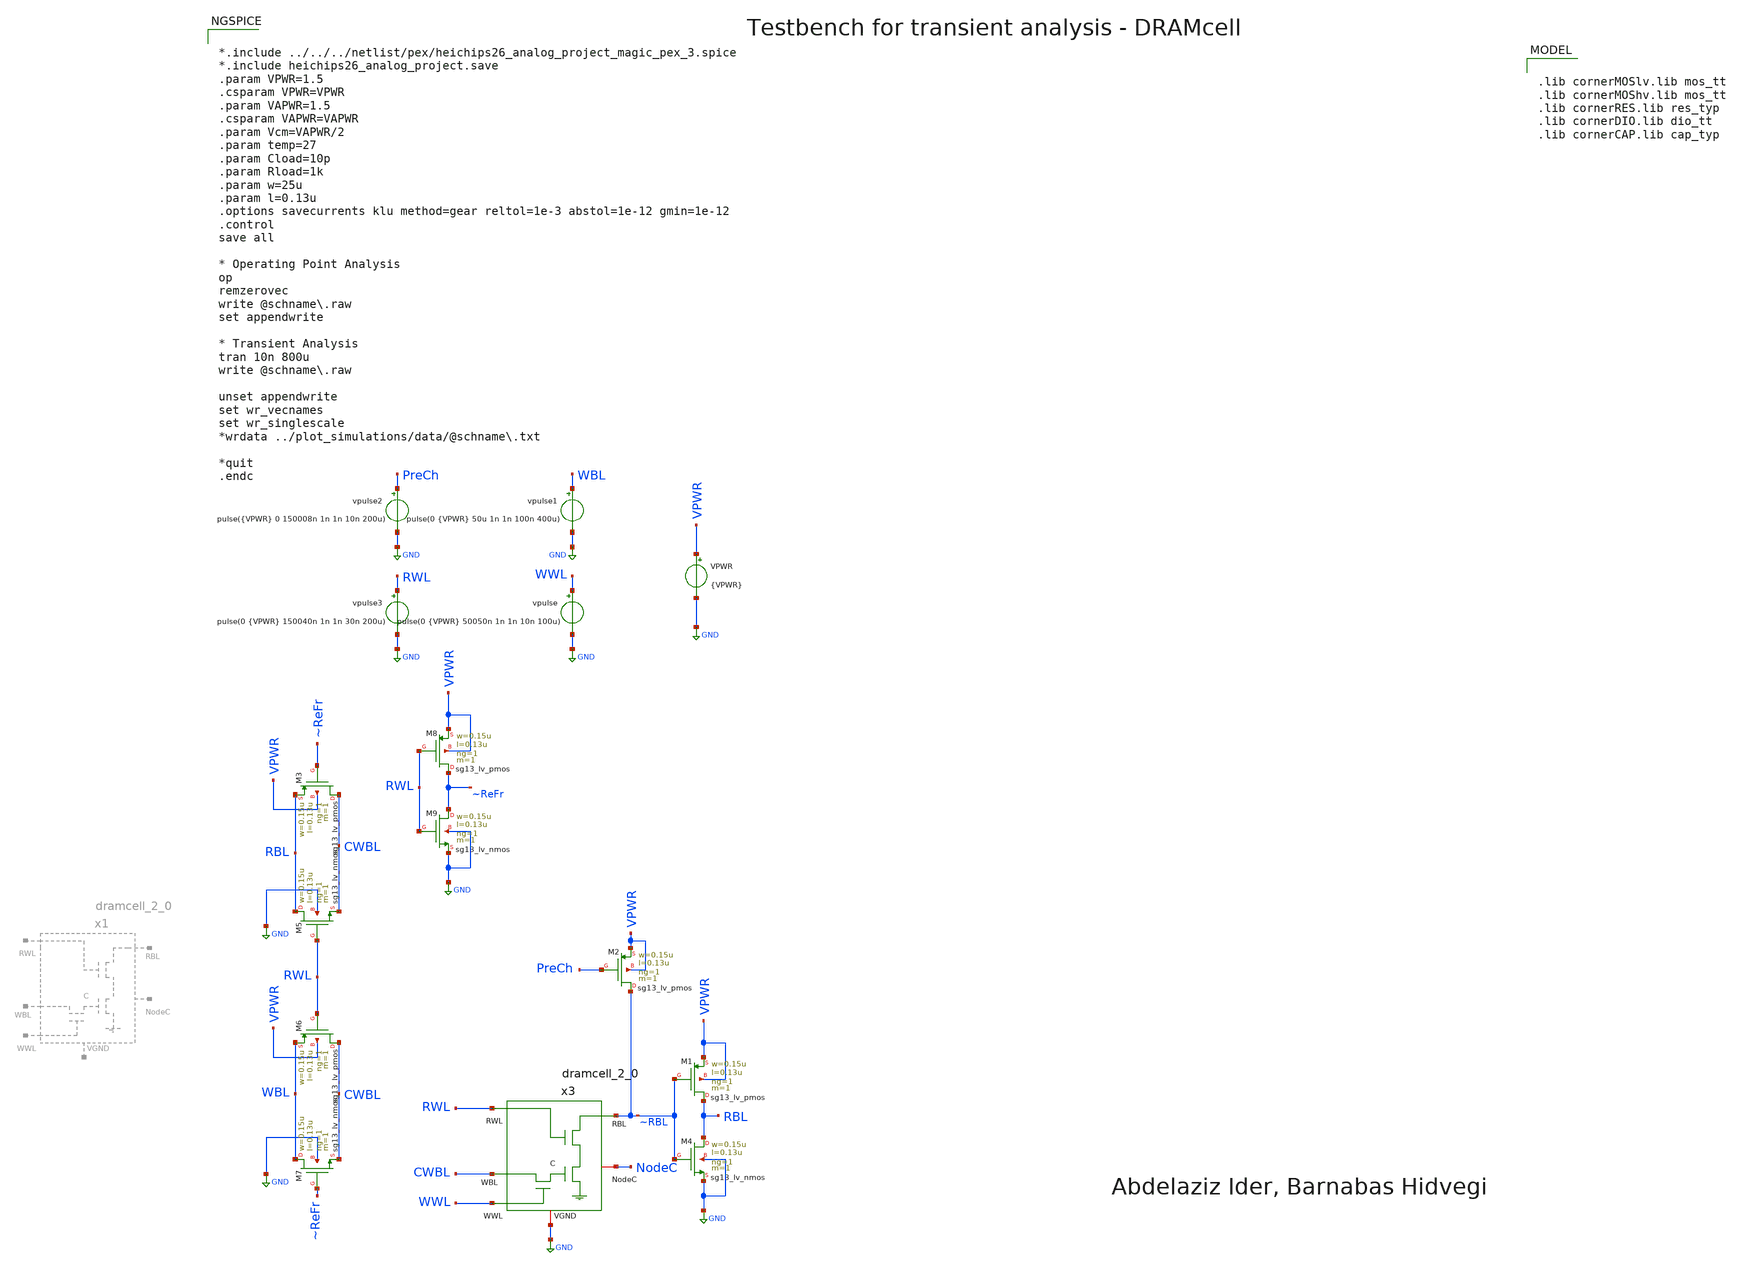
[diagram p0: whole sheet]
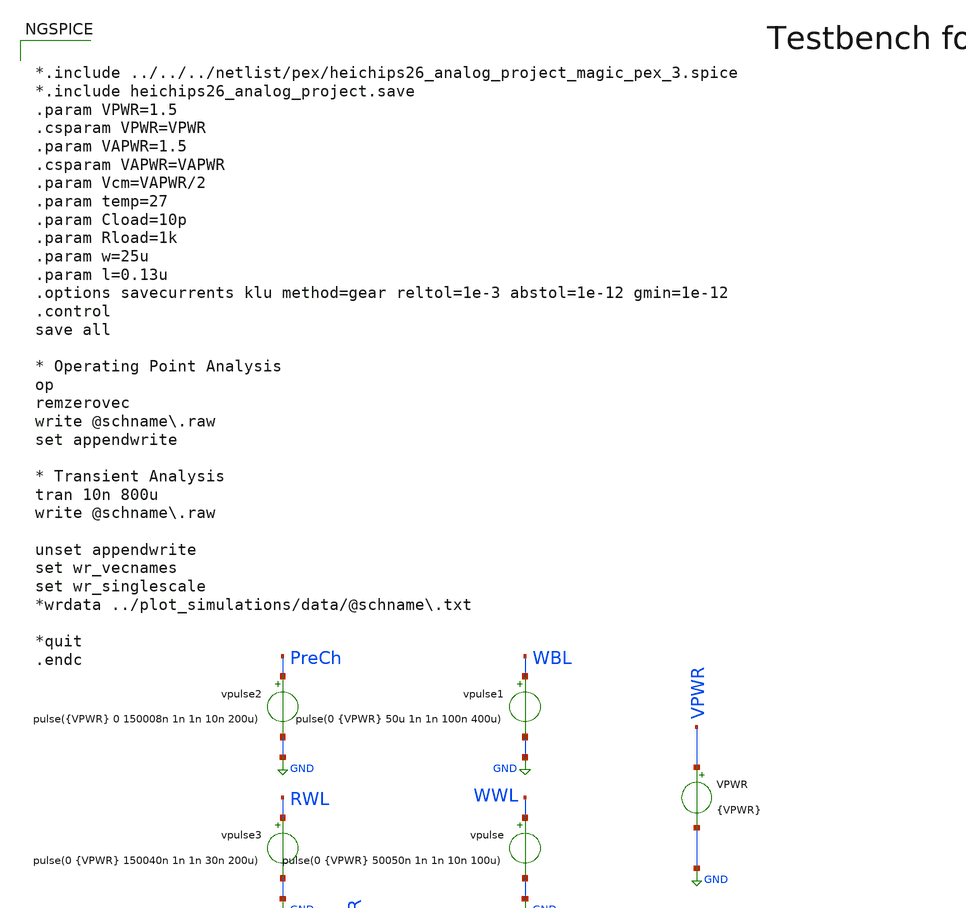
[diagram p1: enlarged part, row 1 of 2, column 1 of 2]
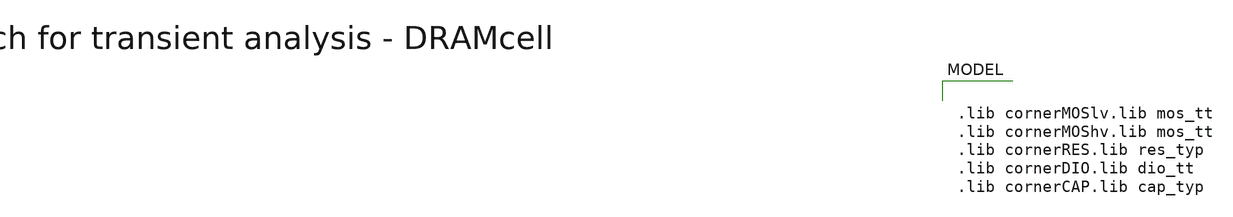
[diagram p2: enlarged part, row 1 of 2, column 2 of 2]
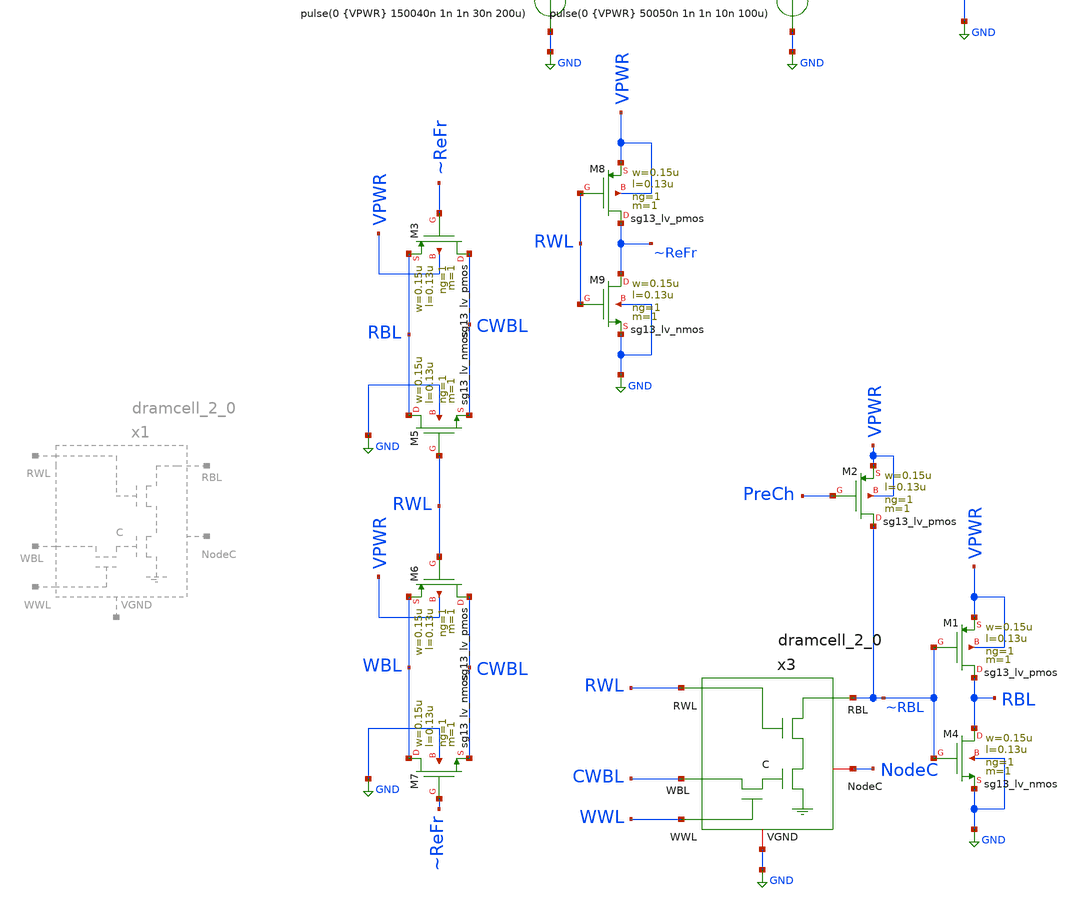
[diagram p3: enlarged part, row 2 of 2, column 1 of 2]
** sch_path: macros/heichips26_analog_project/macros/dramcell_2_0/testbenches/xschem/inverter_tb_tran.sch
**.subckt inverter_tb_tran
vpulse WWL GND pulse(0 {VPWR} 50050n 1n 1n 10n 100u)
VPWR VPWR GND {VPWR}
vpulse1 WBL GND pulse(0 {VPWR} 50u 1n 1n 100n 400u)
vpulse3 RWL GND pulse(0 {VPWR} 150040n 1n 1n 30n 200u)
x3 WWL CWBL RWL ~RBL GND NodeC dramcell_2_0
XM1 RBL ~RBL VPWR VPWR sg13_lv_pmos w=0.15u l=0.13u ng=1 m=1 mm_ok=1
XM4 RBL ~RBL GND GND sg13_lv_nmos w=0.15u l=0.13u ng=1 m=1 mm_ok=1
XM6 CWBL RWL WBL VPWR sg13_lv_pmos w=0.15u l=0.13u ng=1 m=1 mm_ok=1
XM7 WBL ~ReFr CWBL GND sg13_lv_nmos w=0.15u l=0.13u ng=1 m=1 mm_ok=1
XM8 ~ReFr RWL VPWR VPWR sg13_lv_pmos w=0.15u l=0.13u ng=1 m=1 mm_ok=1
XM9 ~ReFr RWL GND GND sg13_lv_nmos w=0.15u l=0.13u ng=1 m=1 mm_ok=1
XM3 CWBL ~ReFr RBL VPWR sg13_lv_pmos w=0.15u l=0.13u ng=1 m=1 mm_ok=1
XM5 RBL RWL CWBL GND sg13_lv_nmos w=0.15u l=0.13u ng=1 m=1 mm_ok=1
XM2 ~RBL PreCh VPWR VPWR sg13_lv_pmos w=0.15u l=0.13u ng=1 m=1 mm_ok=1
vpulse2 PreCh GND pulse({VPWR} 0 150008n 1n 1n 10n 200u)
**** begin user architecture code


*.include ../../../netlist/pex/heichips26_analog_project_magic_pex_3.spice
*.include heichips26_analog_project.save
.param VPWR=1.5
.csparam VPWR=VPWR
.param VAPWR=1.5
.csparam VAPWR=VAPWR
.param Vcm=VAPWR/2
.param temp=27
.param Cload=10p
.param Rload=1k
.param w=25u
.param l=0.13u
.options savecurrents klu method=gear reltol=1e-3 abstol=1e-12 gmin=1e-12
.control
save all

* Operating Point Analysis
op
remzerovec
write @schname\.raw
set appendwrite

* Transient Analysis
tran 10n 800u
write @schname\.raw

unset appendwrite
set wr_vecnames
set wr_singlescale
*wrdata ../plot_simulations/data/@schname\.txt

*quit
.endc



.lib cornerMOSlv.lib mos_tt
.lib cornerMOShv.lib mos_tt
.lib cornerRES.lib res_typ
.lib cornerDIO.lib dio_tt
.lib cornerCAP.lib cap_typ

**** end user architecture code
**.ends
.GLOBAL GND
.end
